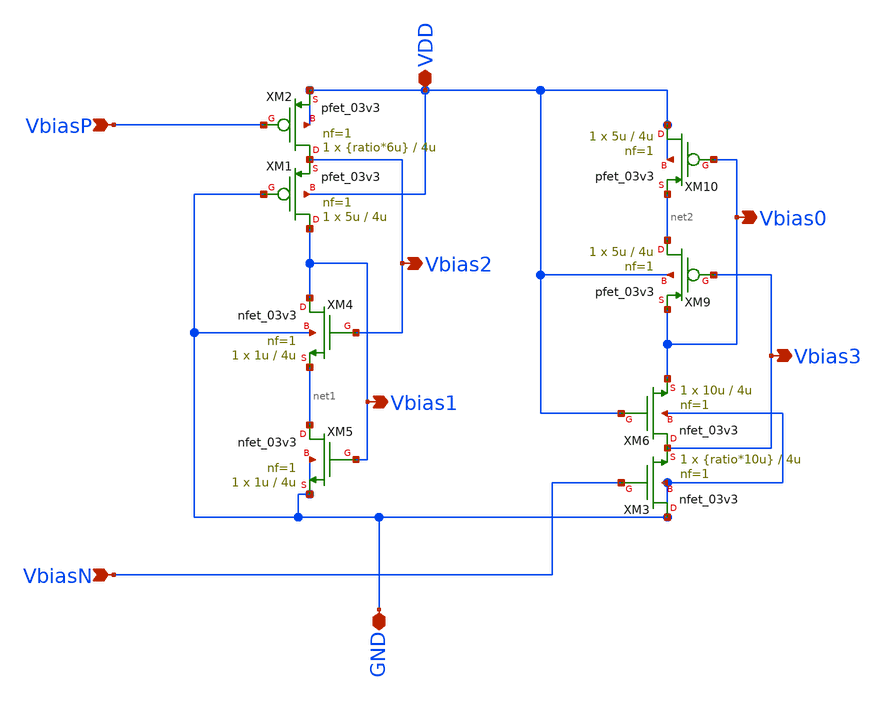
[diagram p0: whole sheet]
** sch_path: analog/B04_OTA_bias_core_old.sch
**.subckt B04_OTA_bias_core_old VDD Vbias2 Vbias1 Vbias0 Vbias3 GND VbiasP VbiasN
*.iopin VDD
*.opin Vbias2
*.opin Vbias1
*.opin Vbias0
*.opin Vbias3
*.iopin GND
*.ipin VbiasP
*.ipin VbiasN
XM1 Vbias1 GND Vbias2 VDD pfet_03v3 L=4u W=5u nf=1 ad='int((nf+1)/2) * W/nf * 0.18u' as='int((nf+2)/2) * W/nf * 0.18u'
+ pd='2*int((nf+1)/2) * (W/nf + 0.18u)' ps='2*int((nf+2)/2) * (W/nf + 0.18u)' nrd='0.18u / W' nrs='0.18u / W'
+ sa=0 sb=0 sd=0 m=1
XM4 Vbias1 Vbias2 net1 GND nfet_03v3 L=4u W=1u nf=1 ad='int((nf+1)/2) * W/nf * 0.18u' as='int((nf+2)/2) * W/nf * 0.18u'
+ pd='2*int((nf+1)/2) * (W/nf + 0.18u)' ps='2*int((nf+2)/2) * (W/nf + 0.18u)' nrd='0.18u / W' nrs='0.18u / W'
+ sa=0 sb=0 sd=0 m=1
XM5 net1 Vbias1 GND GND nfet_03v3 L=4u W=1u nf=1 ad='int((nf+1)/2) * W/nf * 0.18u' as='int((nf+2)/2) * W/nf * 0.18u'
+ pd='2*int((nf+1)/2) * (W/nf + 0.18u)' ps='2*int((nf+2)/2) * (W/nf + 0.18u)' nrd='0.18u / W' nrs='0.18u / W'
+ sa=0 sb=0 sd=0 m=1
XM9 net2 Vbias3 Vbias0 VDD pfet_03v3 L=4u W=5u nf=1 ad='int((nf+1)/2) * W/nf * 0.18u' as='int((nf+2)/2) * W/nf * 0.18u'
+ pd='2*int((nf+1)/2) * (W/nf + 0.18u)' ps='2*int((nf+2)/2) * (W/nf + 0.18u)' nrd='0.18u / W' nrs='0.18u / W'
+ sa=0 sb=0 sd=0 m=1
XM10 VDD Vbias0 net2 VDD pfet_03v3 L=4u W=5u nf=1 ad='int((nf+1)/2) * W/nf * 0.18u' as='int((nf+2)/2) * W/nf * 0.18u'
+ pd='2*int((nf+1)/2) * (W/nf + 0.18u)' ps='2*int((nf+2)/2) * (W/nf + 0.18u)' nrd='0.18u / W' nrs='0.18u / W'
+ sa=0 sb=0 sd=0 m=1
XM6 Vbias3 VDD Vbias0 GND nfet_03v3 L=4u W=10u nf=1 ad='int((nf+1)/2) * W/nf * 0.18u' as='int((nf+2)/2) * W/nf * 0.18u'
+ pd='2*int((nf+1)/2) * (W/nf + 0.18u)' ps='2*int((nf+2)/2) * (W/nf + 0.18u)' nrd='0.18u / W' nrs='0.18u / W'
+ sa=0 sb=0 sd=0 m=1
XM2 Vbias2 VbiasP VDD VDD pfet_03v3 L=4u W={ratio*6u} nf=1 ad='int((nf+1)/2) * W/nf * 0.18u' as='int((nf+2)/2) * W/nf * 0.18u'
+ pd='2*int((nf+1)/2) * (W/nf + 0.18u)' ps='2*int((nf+2)/2) * (W/nf + 0.18u)' nrd='0.18u / W' nrs='0.18u / W'
+ sa=0 sb=0 sd=0 m=1
XM3 GND VbiasN Vbias3 GND nfet_03v3 L=4u W={ratio*10u} nf=1 ad='int((nf+1)/2) * W/nf * 0.18u' as='int((nf+2)/2) * W/nf * 0.18u'
+ pd='2*int((nf+1)/2) * (W/nf + 0.18u)' ps='2*int((nf+2)/2) * (W/nf + 0.18u)' nrd='0.18u / W' nrs='0.18u / W'
+ sa=0 sb=0 sd=0 m=1
**.ends
.end
